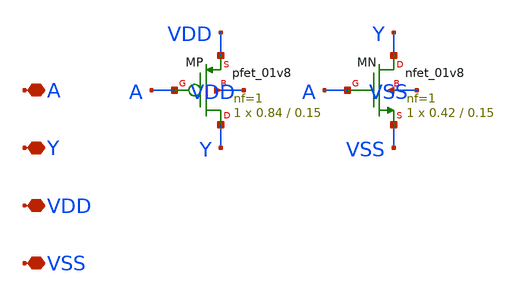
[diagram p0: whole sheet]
** sch_path: design/compiler/cells/sram_inv.sch
**.subckt sram_inv A Y VDD VSS
*.iopin A
*.iopin Y
*.iopin VDD
*.iopin VSS
XMP Y A VDD VDD sky130_fd_pr__pfet_01v8 L=0.15 W=0.84 nf=1 ad=0.2436 as=0.2436 pd=2.26 ps=2.26
+ nrd=0.3452 nrs=0.3452 sa=0 sb=0 sd=0 mult=1 m=1
XMN Y A VSS VSS sky130_fd_pr__nfet_01v8 L=0.15 W=0.42 nf=1 ad=0.1218 as=0.1218 pd=1.42 ps=1.42
+ nrd=0.6905 nrs=0.6905 sa=0 sb=0 sd=0 mult=1 m=1
**.ends
.end
